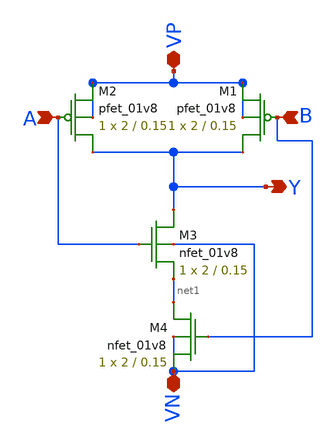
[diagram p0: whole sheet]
** sch_path: Miniproject1/NAND.sch
**.subckt NAND Y A B VP VN
*.opin Y
*.ipin A
*.ipin B
*.iopin VP
*.iopin VN
XM2 Y A VP VP sky130_fd_pr__pfet_01v8 L=0.15 W=2 nf=1 ad='int((nf+1)/2) * W/nf * 0.29' as='int((nf+2)/2) * W/nf * 0.29'
+ pd='2*int((nf+1)/2) * (W/nf + 0.29)' ps='2*int((nf+2)/2) * (W/nf + 0.29)' nrd='0.29 / W' nrs='0.29 / W'
+ sa=0 sb=0 sd=0 mult=1 m=1
XM1 Y B VP VP sky130_fd_pr__pfet_01v8 L=0.15 W=2 nf=1 ad='int((nf+1)/2) * W/nf * 0.29' as='int((nf+2)/2) * W/nf * 0.29'
+ pd='2*int((nf+1)/2) * (W/nf + 0.29)' ps='2*int((nf+2)/2) * (W/nf + 0.29)' nrd='0.29 / W' nrs='0.29 / W'
+ sa=0 sb=0 sd=0 mult=1 m=1
XM3 Y A net1 VN sky130_fd_pr__nfet_01v8 L=0.15 W=2 nf=1 ad='int((nf+1)/2) * W/nf * 0.29' as='int((nf+2)/2) * W/nf * 0.29'
+ pd='2*int((nf+1)/2) * (W/nf + 0.29)' ps='2*int((nf+2)/2) * (W/nf + 0.29)' nrd='0.29 / W' nrs='0.29 / W'
+ sa=0 sb=0 sd=0 mult=1 m=1
XM4 net1 B VN VN sky130_fd_pr__nfet_01v8 L=0.15 W=2 nf=1 ad='int((nf+1)/2) * W/nf * 0.29' as='int((nf+2)/2) * W/nf * 0.29'
+ pd='2*int((nf+1)/2) * (W/nf + 0.29)' ps='2*int((nf+2)/2) * (W/nf + 0.29)' nrd='0.29 / W' nrs='0.29 / W'
+ sa=0 sb=0 sd=0 mult=1 m=1
**.ends
.end
